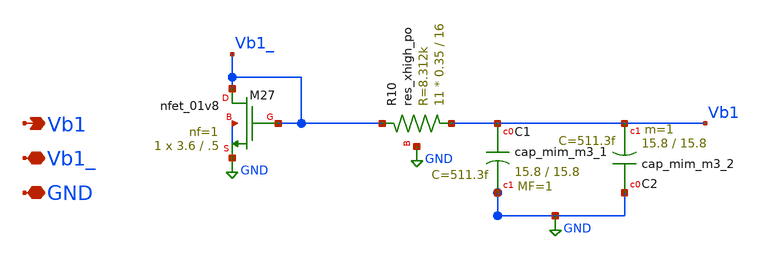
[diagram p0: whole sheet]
** sch_path: schem/mirror_1.sch
**.subckt mirror_1 GND Vb1_ Vb1
*.iopin GND
*.iopin Vb1_
*.opin Vb1
XM27 Vb1_ Vb1_ GND GND sky130_fd_pr__nfet_01v8 L=.5 W=3.6 nf=1 ad='int((nf+1)/2) * W/nf * 0.29' as='int((nf+2)/2) * W/nf * 0.29'
+ pd='2*int((nf+1)/2) * (W/nf + 0.29)' ps='2*int((nf+2)/2) * (W/nf + 0.29)' nrd='0.29 / W' nrs='0.29 / W'
+ sa=0 sb=0 sd=0 mult=1 m=1
XC1 Vb1 GND sky130_fd_pr__cap_mim_m3_1 W=15.8 L=15.8 MF=1 m=1
XC2 GND Vb1 sky130_fd_pr__cap_mim_m3_2 W=15.8 L=15.8 MF=1 m=1
XR10 Vb1 Vb1_ GND sky130_fd_pr__res_xhigh_po W=0.35 L=16 mult=11 m=11
**.ends
.GLOBAL GND
.end
